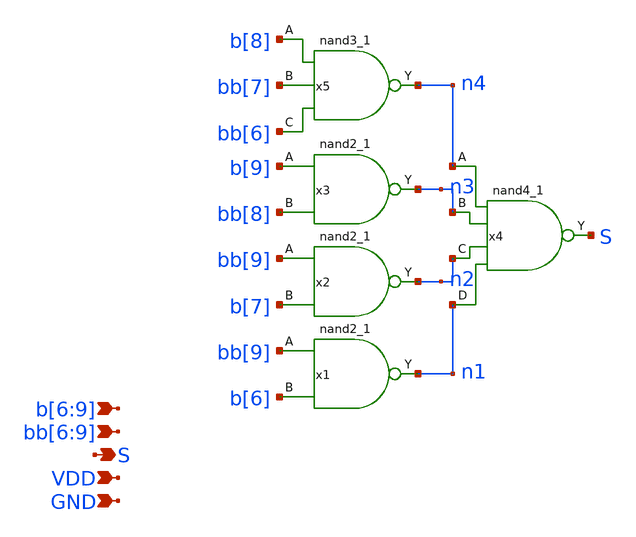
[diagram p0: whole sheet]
** sch_path: xschem/seg_selector_2_logic.sch
**.subckt seg_selector_2_logic b[6],b[7],b[8],b[9] S GND VDD bb[6],bb[7],bb[8],bb[9]
*.ipin b[6],b[7],b[8],b[9]
*.opin S
*.ipin GND
*.ipin VDD
*.ipin bb[6],bb[7],bb[8],bb[9]
x1 bb[9] b[6] GND GND VDD VDD n1 sky130_fd_sc_hd__nand2_1
x2 bb[9] b[7] GND GND VDD VDD n2 sky130_fd_sc_hd__nand2_1
x3 b[9] bb[8] GND GND VDD VDD n3 sky130_fd_sc_hd__nand2_1
x5 b[8] bb[7] bb[6] GND GND VDD VDD n4 sky130_fd_sc_hd__nand3_1
x4 n4 n3 n2 n1 GND GND VDD VDD S sky130_fd_sc_hd__nand4_1
**.ends
.end
